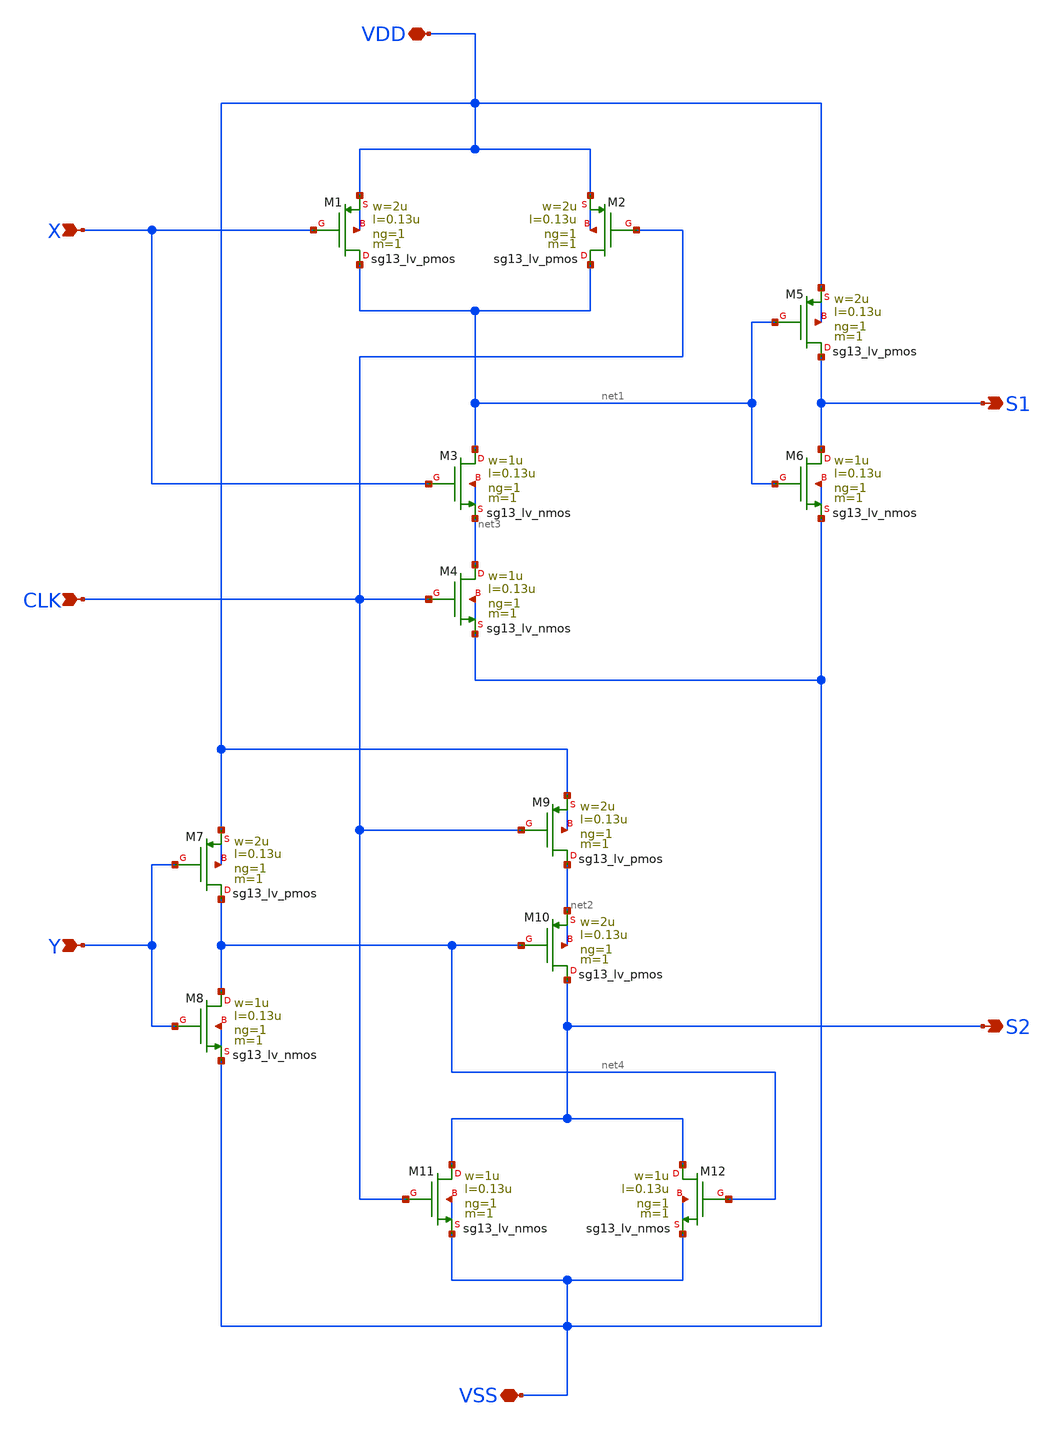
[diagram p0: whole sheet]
** sch_path: SSDOR_1.2V_v2/components/logic_contorller/logic_controller.sch
**.subckt logic_controller X CLK Y S1 S2 VSS VDD
*.ipin X
*.ipin CLK
*.ipin Y
*.opin S1
*.opin S2
*.iopin VSS
*.iopin VDD
XM1 net1 X VDD VDD sg13_lv_pmos w=2u l=0.13u ng=1 m=1 mm_ok=1
XM2 net1 CLK VDD VDD sg13_lv_pmos w=2u l=0.13u ng=1 m=1 mm_ok=1
XM3 net1 X net3 net3 sg13_lv_nmos w=1u l=0.13u ng=1 m=1 mm_ok=1
XM4 net3 CLK VSS VSS sg13_lv_nmos w=1u l=0.13u ng=1 m=1 mm_ok=1
XM5 S1 net1 VDD VDD sg13_lv_pmos w=2u l=0.13u ng=1 m=1 mm_ok=1
XM6 S1 net1 VSS VSS sg13_lv_nmos w=1u l=0.13u ng=1 m=1 mm_ok=1
XM7 net4 Y VDD VDD sg13_lv_pmos w=2u l=0.13u ng=1 m=1 mm_ok=1
XM8 net4 Y VSS VSS sg13_lv_nmos w=1u l=0.13u ng=1 m=1 mm_ok=1
XM9 net2 CLK VDD VDD sg13_lv_pmos w=2u l=0.13u ng=1 m=1 mm_ok=1
XM10 S2 net4 net2 net2 sg13_lv_pmos w=2u l=0.13u ng=1 m=1 mm_ok=1
XM11 S2 CLK VSS VSS sg13_lv_nmos w=1u l=0.13u ng=1 m=1 mm_ok=1
XM12 S2 net4 VSS VSS sg13_lv_nmos w=1u l=0.13u ng=1 m=1 mm_ok=1
**.ends
.end
